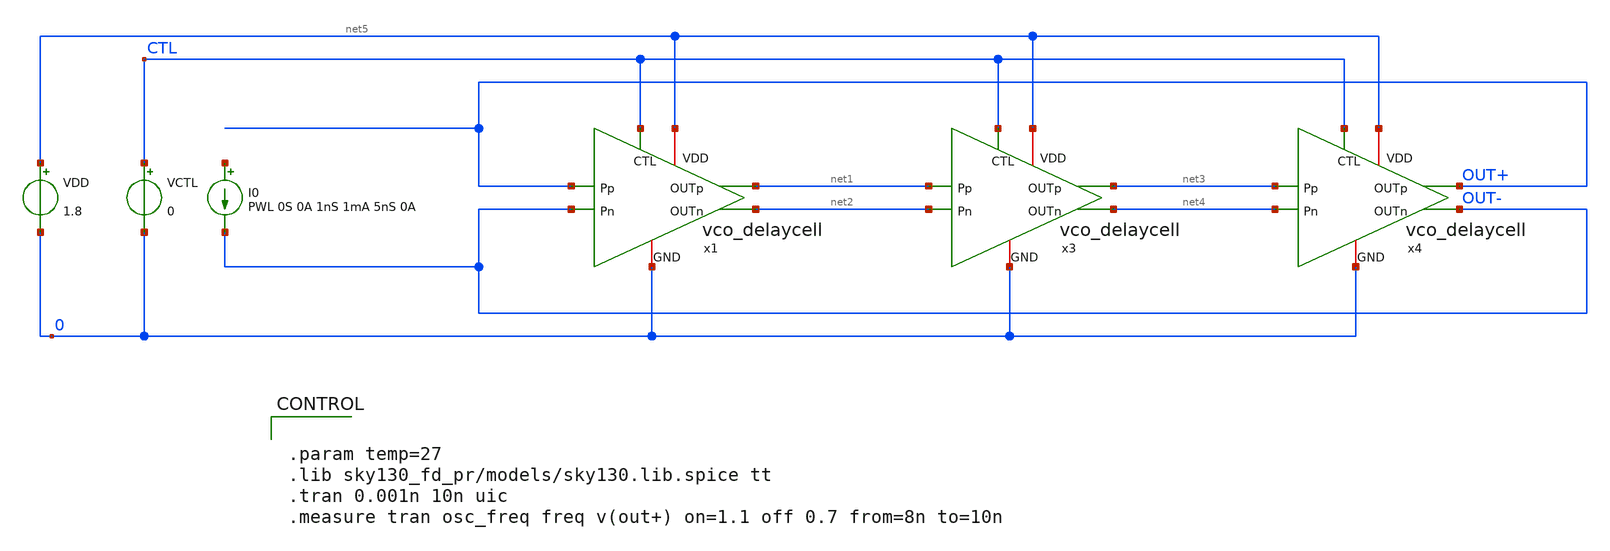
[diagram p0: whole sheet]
** sch_path: design/vco_2-4GHz_delaycell/tests/vco_delaycell_3cells_tb.sch
**.subckt vco_delaycell_3cells_tb
x1 net5 net2 net1 OUT- OUT+ 0 CTL vco_delaycell
VDD net5 0 1.8
VCTL CTL 0 0
x3 net5 net4 net3 net2 net1 0 CTL vco_delaycell
x4 net5 OUT- OUT+ net4 net3 0 CTL vco_delaycell
I0 net6 OUT- PWL 0S 0A 1nS 1mA 5nS 0A
**** begin user architecture code


.param temp=27
.lib sky130_fd_pr/models/sky130.lib.spice tt
.tran 0.001n 10n uic
.measure tran osc_freq freq v(out+) on=1.1 off 0.7 from=8n to=10n


**** end user architecture code
**.ends

* expanding   symbol:  vco_delaycell/vco_delaycell.sym # of pins=7
** sym_path: design/vco_delaycell/vco_delaycell.sym
** sch_path: design/vco_delaycell/vco_delaycell.sch
.subckt vco_delaycell VDD OUTn OUTp Pn Pp GND CTL
*.ipin Pp
*.ipin Pn
*.opin OUTn
*.opin OUTp
*.iopin VDD
*.iopin GND
*.ipin CTL
XXMprimpos OUTp Pp GND GND sky130_fd_pr__rf_nfet_01v8_bM04W5p00L0p15 m=3
XXMcrossneg OUTn OUTp GND GND sky130_fd_pr__rf_nfet_01v8_bM02W1p65L0p15 m=1
XXMctlneg OUTn CTL VDD VDD sky130_fd_pr__rf_pfet_01v8_aF02W5p00L0p15 m=2
XXMctlpos OUTp CTL VDD VDD sky130_fd_pr__rf_pfet_01v8_aF02W5p00L0p15 m=2
XXMcrosspos OUTp OUTn GND GND sky130_fd_pr__rf_nfet_01v8_bM02W1p65L0p15 m=1
XXMprimneg OUTn Pn GND GND sky130_fd_pr__rf_nfet_01v8_bM04W5p00L0p15 m=3
XXMctlpos1 OUTp GND VDD VDD sky130_fd_pr__rf_pfet_01v8_aF02W0p84L0p15 m=1
XXMctlneg1 OUTn GND VDD VDD sky130_fd_pr__rf_pfet_01v8_aF02W0p84L0p15 m=1
.ends

.end
